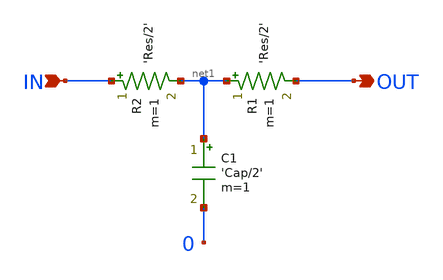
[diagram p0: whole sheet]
** sch_path: tests/test_sweep_diff/examples/rcline/schematic/rcline.sch
* Copyright (C) 1998-2024 Stefan Frederik Schippers
* This program is free software; you can redistribute it and/or modify
* it under the terms of the GNU General Public License as published by
* the Free Software Foundation; either version 2 of the License, or
* (at your option) any later version.
* This program is distributed in the hope that it will be useful,
* but WITHOUT ANY WARRANTY; without even the implied warranty of
* MERCHANTABILITY or FITNESS FOR A PARTICULAR PURPOSE.  See the
* GNU General Public License for more details.
* You should have received a copy of the GNU General Public License
* along with this program; if not, write to the Free Software
**.subckt rcline IN OUT
*.ipin IN
*.opin OUT
C1 net1 0 'Cap/2' m=1
R1 net1 OUT 'Res/2' m=1
R2 IN net1 'Res/2' m=1
**.ends
.end
